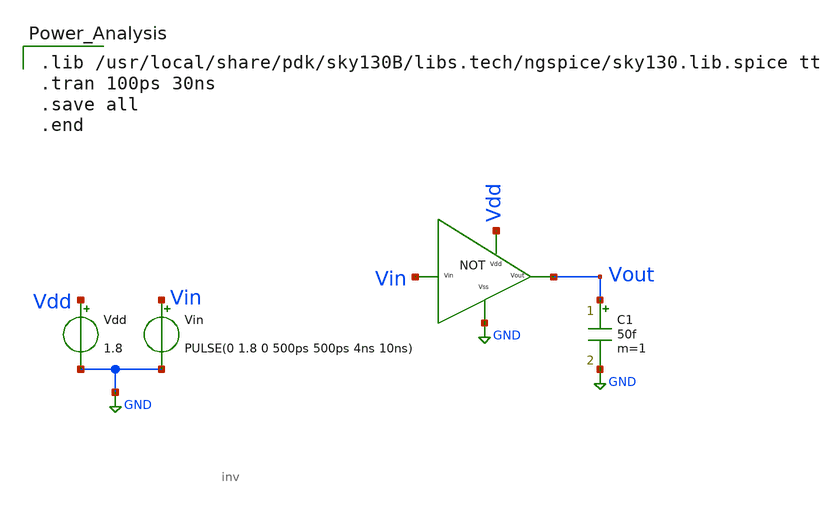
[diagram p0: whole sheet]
** sch_path: Xschem/power.sch
**.subckt power
x1 Vdd Vin Vout GND inv
Vdd Vdd GND 1.8
Vin Vin GND PULSE(0 1.8 0 500ps 500ps 4ns 10ns)
C1 Vout GND 50f m=1
**** begin user architecture code

.lib /usr/local/share/pdk/sky130B/libs.tech/ngspice/sky130.lib.spice tt
.tran 100ps 30ns
.save all
.end

**** end user architecture code
**.ends

* expanding   symbol:  inv.sym # of pins=4
** sym_path: Xschem/inv.sym
** sch_path: Xschem/inv.sch
.subckt inv Vdd Vin Vout Vss
*.ipin Vin
*.ipin Vss
*.ipin Vdd
*.opin Vout
XM1 Vout Vin Vss GND sky130_fd_pr__nfet_01v8 L=0.15 W=1 nf=1 ad='int((nf+1)/2) * W/nf * 0.29' as='int((nf+2)/2) * W/nf * 0.29'
+ pd='2*int((nf+1)/2) * (W/nf + 0.29)' ps='2*int((nf+2)/2) * (W/nf + 0.29)' nrd='0.29 / W' nrs='0.29 / W'
+ sa=0 sb=0 sd=0 mult=1 m=1
XM2 Vout Vin Vdd VDD sky130_fd_pr__pfet_01v8 L=0.15 W=2.5 nf=1 ad='int((nf+1)/2) * W/nf * 0.29' as='int((nf+2)/2) * W/nf * 0.29'
+ pd='2*int((nf+1)/2) * (W/nf + 0.29)' ps='2*int((nf+2)/2) * (W/nf + 0.29)' nrd='0.29 / W' nrs='0.29 / W'
+ sa=0 sb=0 sd=0 mult=1 m=1
.ends

.GLOBAL GND
.end
